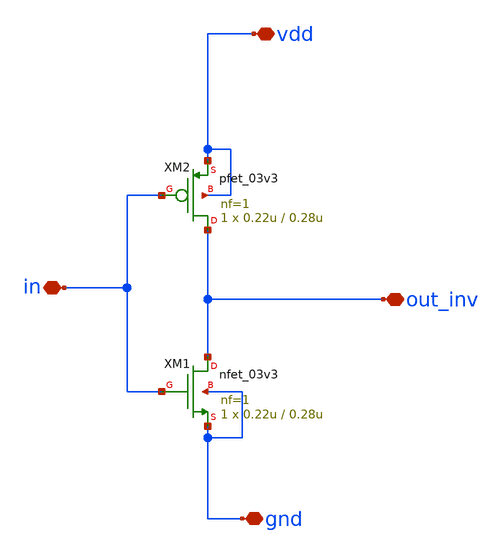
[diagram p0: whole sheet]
** sch_path: designs/schematics/mux2x1_transmission_gate/mux_ctrl_logic.sch
**.subckt mux_ctrl_logic vdd gnd out_inv in
*.iopin vdd
*.iopin gnd
*.iopin out_inv
*.iopin in
XM1 out_inv in gnd gnd nfet_03v3 L=0.28u W=0.22u nf=1 ad='int((nf+1)/2) * W/nf * 0.18u' as='int((nf+2)/2) * W/nf * 0.18u'
+ pd='2*int((nf+1)/2) * (W/nf + 0.18u)' ps='2*int((nf+2)/2) * (W/nf + 0.18u)' nrd='0.18u / W' nrs='0.18u / W'
+ sa=0 sb=0 sd=0 m=1
XM2 out_inv in vdd vdd pfet_03v3 L=0.28u W=0.22u nf=1 ad='int((nf+1)/2) * W/nf * 0.18u' as='int((nf+2)/2) * W/nf * 0.18u'
+ pd='2*int((nf+1)/2) * (W/nf + 0.18u)' ps='2*int((nf+2)/2) * (W/nf + 0.18u)' nrd='0.18u / W' nrs='0.18u / W'
+ sa=0 sb=0 sd=0 m=1
**.ends
.end
